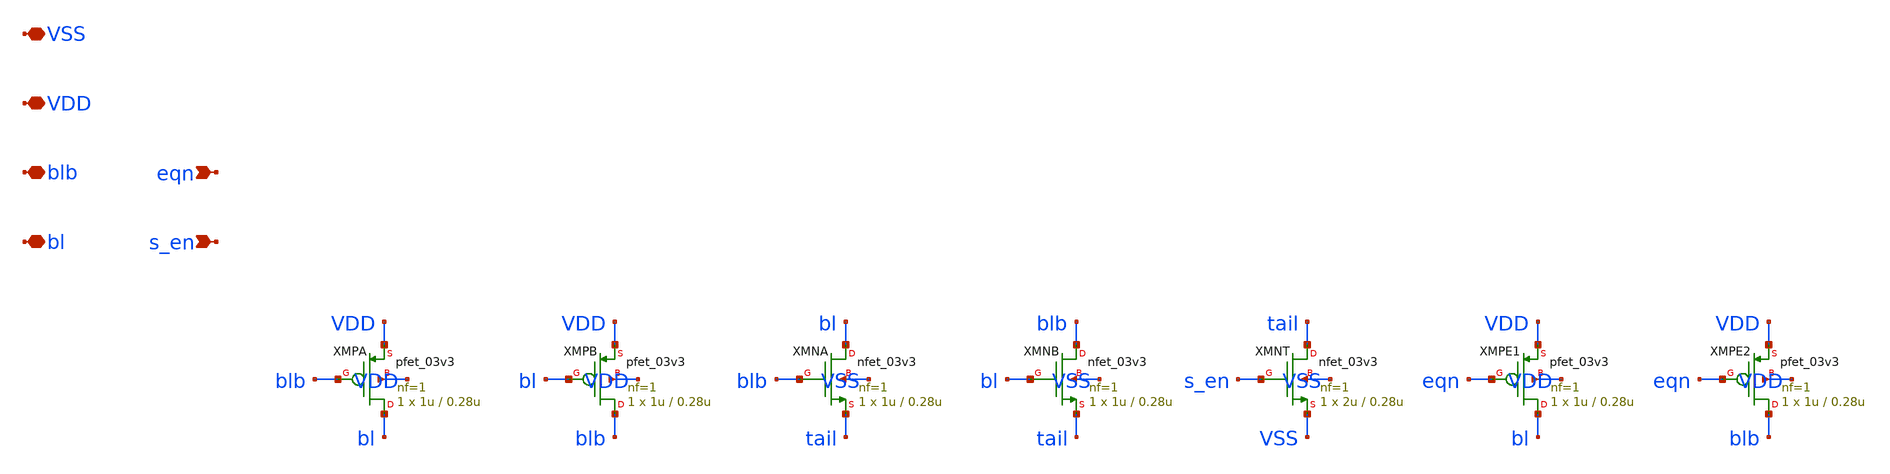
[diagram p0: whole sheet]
** sch_path: design/sa_latch.sch
**.subckt sa_latch s_en eqn bl blb VDD VSS
*.ipin s_en
*.ipin eqn
*.iopin bl
*.iopin blb
*.iopin VDD
*.iopin VSS
XMPA bl blb VDD VDD pfet_03v3 L=0.28u W=1u nf=1 ad='int((nf+1)/2) * W/nf * 0.18u' as='int((nf+2)/2) * W/nf * 0.18u'
+ pd='2*int((nf+1)/2) * (W/nf + 0.18u)' ps='2*int((nf+2)/2) * (W/nf + 0.18u)' nrd='0.18u / W' nrs='0.18u / W'
+ sa=0 sb=0 sd=0 m=1
XMPB blb bl VDD VDD pfet_03v3 L=0.28u W=1u nf=1 ad='int((nf+1)/2) * W/nf * 0.18u' as='int((nf+2)/2) * W/nf * 0.18u'
+ pd='2*int((nf+1)/2) * (W/nf + 0.18u)' ps='2*int((nf+2)/2) * (W/nf + 0.18u)' nrd='0.18u / W' nrs='0.18u / W'
+ sa=0 sb=0 sd=0 m=1
XMNA bl blb tail VSS nfet_03v3 L=0.28u W=1u nf=1 ad='int((nf+1)/2) * W/nf * 0.18u' as='int((nf+2)/2) * W/nf * 0.18u'
+ pd='2*int((nf+1)/2) * (W/nf + 0.18u)' ps='2*int((nf+2)/2) * (W/nf + 0.18u)' nrd='0.18u / W' nrs='0.18u / W'
+ sa=0 sb=0 sd=0 m=1
XMNB blb bl tail VSS nfet_03v3 L=0.28u W=1u nf=1 ad='int((nf+1)/2) * W/nf * 0.18u' as='int((nf+2)/2) * W/nf * 0.18u'
+ pd='2*int((nf+1)/2) * (W/nf + 0.18u)' ps='2*int((nf+2)/2) * (W/nf + 0.18u)' nrd='0.18u / W' nrs='0.18u / W'
+ sa=0 sb=0 sd=0 m=1
XMNT tail s_en VSS VSS nfet_03v3 L=0.28u W=2u nf=1 ad='int((nf+1)/2) * W/nf * 0.18u' as='int((nf+2)/2) * W/nf * 0.18u'
+ pd='2*int((nf+1)/2) * (W/nf + 0.18u)' ps='2*int((nf+2)/2) * (W/nf + 0.18u)' nrd='0.18u / W' nrs='0.18u / W'
+ sa=0 sb=0 sd=0 m=1
XMPE1 bl eqn VDD VDD pfet_03v3 L=0.28u W=1u nf=1 ad='int((nf+1)/2) * W/nf * 0.18u' as='int((nf+2)/2) * W/nf * 0.18u'
+ pd='2*int((nf+1)/2) * (W/nf + 0.18u)' ps='2*int((nf+2)/2) * (W/nf + 0.18u)' nrd='0.18u / W' nrs='0.18u / W'
+ sa=0 sb=0 sd=0 m=1
XMPE2 blb eqn VDD VDD pfet_03v3 L=0.28u W=1u nf=1 ad='int((nf+1)/2) * W/nf * 0.18u' as='int((nf+2)/2) * W/nf * 0.18u'
+ pd='2*int((nf+1)/2) * (W/nf + 0.18u)' ps='2*int((nf+2)/2) * (W/nf + 0.18u)' nrd='0.18u / W' nrs='0.18u / W'
+ sa=0 sb=0 sd=0 m=1
**.ends
.end
